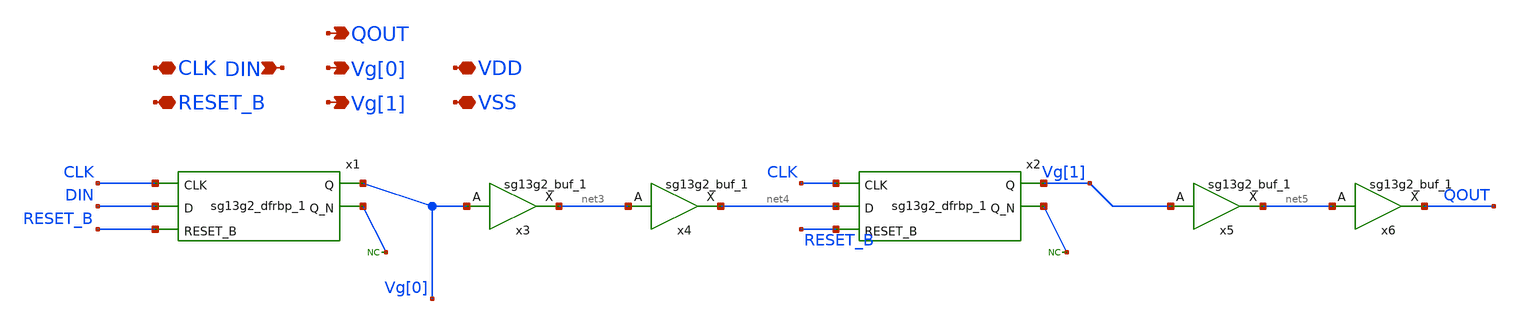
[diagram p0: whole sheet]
** sch_path: ihp130_cells/ShiftRegister/ShiftRegister.sch
* IHP-GmbH/IHP-Open-PDK/ihp-sg13g2/libs.tech/xschem/sg13g2_stdcells/sg13g2_buf_1.sch:
* Copyright 2023 IHP PDK Authors
* Licensed under the Apache License, Version 2.0 (the "License");
**.subckt ShiftRegister CLK RESET_B DIN Vg[0] Vg[1] VDD VSS QOUT
*.iopin CLK
*.iopin RESET_B
*.ipin DIN
*.opin Vg[0]
*.opin Vg[1]
*.iopin VDD
*.iopin VSS
*.opin QOUT
x1 Vg[0] net1 CLK DIN RESET_B VDD VSS sg13g2_dfrbp_1
x2 Vg[1] net2 CLK net4 RESET_B VDD VSS sg13g2_dfrbp_1
* noconn #net1
* noconn #net2
x3 net3 Vg[0] VDD VSS sg13g2_buf_1
x4 net4 net3 VDD VSS sg13g2_buf_1
x5 net5 Vg[1] VDD VSS sg13g2_buf_1
x6 QOUT net5 VDD VSS sg13g2_buf_1
**.ends

* expanding   symbol:  sg13g2_stdcells/sg13g2_dfrbp_1.sym # of pins=5
** sym_path: sg13g2_stdcells/sg13g2_dfrbp_1.sym
** sch_path: sg13g2_stdcells/sg13g2_dfrbp_1.sch
.subckt sg13g2_dfrbp_1 Q Q_N CLK D RESET_B VDD VSS
*.ipin D
*.ipin RESET_B
*.ipin CLK
*.opin Q
*.opin Q_N
*.iopin VDD
*.iopin VSS
XM1 Db D net10 VSS sg13_lv_nmos w=420.00n l=130.00n ng=1 m=1 mm_ok=1
XM2 net10 RESET_B VSS VSS sg13_lv_nmos w=420.00n l=130.00n ng=1 m=1 mm_ok=1
XM3 net1 clkneg net9 VSS sg13_lv_nmos w=420.00n l=130.00n ng=1 m=1 mm_ok=1
XM4 net9 net1 VSS VSS sg13_lv_nmos w=420.00n l=130.00n ng=1 m=1 mm_ok=1
XM5 net1 net1 net5 VSS sg13_lv_nmos w=420.00n l=130.00n ng=1 m=1 mm_ok=1
XM6 net5 RESET_B VSS VSS sg13_lv_nmos w=420.00n l=130.00n ng=1 m=1 mm_ok=1
XM7 Q_N net1 VSS VSS sg13_lv_nmos w=740.00n l=130.00n ng=1 m=1 mm_ok=1
XM8 net2 net1 VSS VSS sg13_lv_nmos w=740.00n l=130.00n ng=1 m=1 mm_ok=1
XM9 Q net2 VSS VSS sg13_lv_nmos w=740.00n l=130.00n ng=1 m=1 mm_ok=1
XM10 clkneg CLK VSS VSS sg13_lv_nmos w=740.00n l=130.00n ng=1 m=1 mm_ok=1
XM11 clkpos clkneg VSS VSS sg13_lv_nmos w=740.00n l=130.00n ng=1 m=1 mm_ok=1
XM12 Db clkneg net3 VSS sg13_lv_nmos w=420.00n l=130.00n ng=1 m=1 mm_ok=1
XM13 net3 clkpos net8 VSS sg13_lv_nmos w=420.00n l=130.00n ng=1 m=1 mm_ok=1
XM14 net8 net3 net4 VSS sg13_lv_nmos w=420.00n l=130.00n ng=1 m=1 mm_ok=1
XM15 net4 RESET_B VSS VSS sg13_lv_nmos w=420.00n l=130.00n ng=1 m=1 mm_ok=1
XM16 net3 net3 VSS VSS sg13_lv_nmos w=740.00n l=130.00n ng=1 m=1 mm_ok=1
XM17 net3 clkpos net1 VSS sg13_lv_nmos w=740.00n l=130.00n ng=1 m=1 mm_ok=1
XM18 Db RESET_B VDD VDD sg13_lv_pmos w=420.00n l=130.00n ng=1 m=1 mm_ok=1
XM19 Db D VDD VDD sg13_lv_pmos w=420.00n l=130.00n ng=1 m=1 mm_ok=1
XM20 net7 net1 VDD VDD sg13_lv_pmos w=420.00n l=130.00n ng=1 m=1 mm_ok=1
XM21 net1 clkpos net7 VDD sg13_lv_pmos w=420.00n l=130.00n ng=1 m=1 mm_ok=1
XM22 net1 net1 VDD VDD sg13_lv_pmos w=420.00n l=130.00n ng=1 m=1 mm_ok=1
XM23 net1 RESET_B VDD VDD sg13_lv_pmos w=420.00n l=130.00n ng=1 m=1 mm_ok=1
XM24 Q_N net1 VDD VDD sg13_lv_pmos w=1.12u l=130.00n ng=1 m=1 mm_ok=1
XM25 net2 net1 VDD VDD sg13_lv_pmos w=1.12u l=130.00n ng=1 m=1 mm_ok=1
XM26 Q net2 VDD VDD sg13_lv_pmos w=1.12u l=130.00n ng=1 m=1 mm_ok=1
XM27 clkneg CLK VDD VDD sg13_lv_pmos w=1.12u l=130.00n ng=1 m=1 mm_ok=1
XM28 clkpos clkneg VDD VDD sg13_lv_pmos w=1.12u l=130.00n ng=1 m=1 mm_ok=1
XM29 Db clkpos net3 VDD sg13_lv_pmos w=420.00n l=130.00n ng=1 m=1 mm_ok=1
XM30 net6 net3 VDD VDD sg13_lv_pmos w=420.00n l=130.00n ng=1 m=1 mm_ok=1
XM31 net3 clkneg net6 VDD sg13_lv_pmos w=420.00n l=130.00n ng=1 m=1 mm_ok=1
XM32 net3 RESET_B VDD VDD sg13_lv_pmos w=420.00n l=130.00n ng=1 m=1 mm_ok=1
XM33 net3 net3 VDD VDD sg13_lv_pmos w=1.000u l=130.00n ng=1 m=1 mm_ok=1
XM34 net3 clkneg net1 VDD sg13_lv_pmos w=1.000u l=130.00n ng=1 m=1 mm_ok=1
.ends


* expanding   symbol:  sg13g2_stdcells/sg13g2_buf_1.sym # of pins=2
** sym_path: sg13g2_stdcells/sg13g2_buf_1.sym
** sch_path: sg13g2_stdcells/sg13g2_buf_1.sch
.subckt sg13g2_buf_1 X A VDD VSS
*.ipin A
*.opin X
*.iopin VDD
*.iopin VSS
XM1 net1 A VSS VSS sg13_lv_nmos w=550.00n l=130.00n ng=1 m=1 mm_ok=1
XM2 X net1 VSS VSS sg13_lv_nmos w=740.00n l=130.00n ng=1 m=1 mm_ok=1
XM3 net1 A VDD VDD sg13_lv_pmos w=840.00n l=130.00n ng=1 m=1 mm_ok=1
XM4 X net1 VDD VDD sg13_lv_pmos w=1.12u l=130.00n ng=1 m=1 mm_ok=1
.ends

.end
